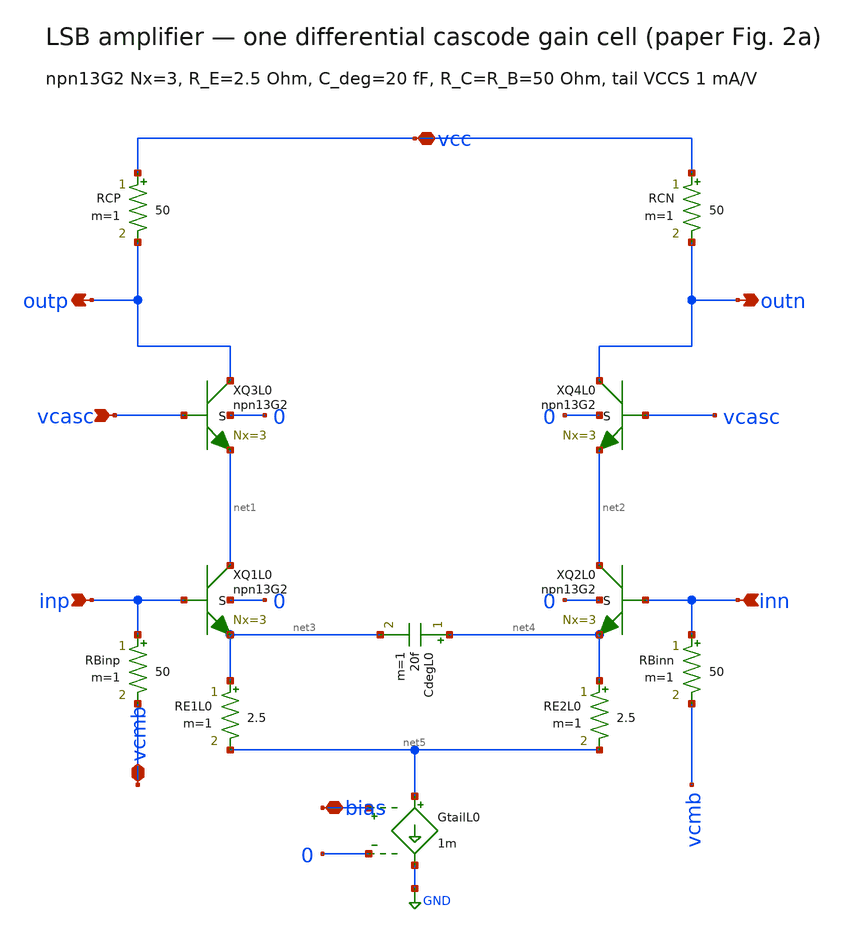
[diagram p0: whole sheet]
** sch_path: analog-db/drawings/pam4-driver-2-bit-dac-HBT/ported-netlists/schematics/dut_lsb.sch
**.subckt dut_lsb vcc outp outn inp inn vcmb bias vcasc
*.iopin vcc
*.opin outp
*.opin outn
*.ipin inp
*.ipin inn
*.iopin vcmb
*.iopin bias
*.ipin vcasc
RCP vcc outp 50 m=1
RCN vcc outn 50 m=1
XQ3L0 outp vcasc net1 0 npn13G2 Nx=3
XQ4L0 outn vcasc net2 0 npn13G2 Nx=3
XQ1L0 net1 inp net3 0 npn13G2 Nx=3
XQ2L0 net2 inn net4 0 npn13G2 Nx=3
CdegL0 net4 net3 20f m=1
RE1L0 net3 net5 2.5 m=1
RE2L0 net4 net5 2.5 m=1
GtailL0 net5 GND bias 0 1m
RBinp inp vcmb 50 m=1
RBinn inn vcmb 50 m=1
**.ends
.GLOBAL GND
.end
